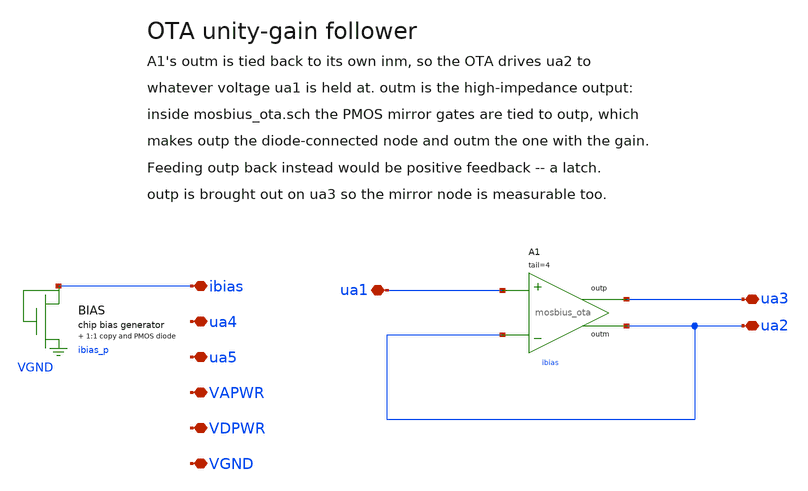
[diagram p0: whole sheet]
** sch_path: examples/otabuf/otabuf.sch
**.subckt otabuf ibias ua1 ua2 ua3 ua4 ua5 VAPWR VDPWR VGND
*.iopin ibias
*.iopin ua1
*.iopin ua2
*.iopin ua3
*.iopin ua4
*.iopin ua5
*.iopin VAPWR
*.iopin VDPWR
*.iopin VGND
XA1 ua1 ua2 ua3 ua2 ibias VGND VAPWR mosbius_ota tail=4
XBIAS ibias ibias_p VGND VAPWR mosbius_bias
**.ends

* expanding   symbol:  mosbius_ota.sym # of pins=4
** sym_path: xschem/mosbius_lib/mosbius_ota.sym
** sch_path: xschem/mosbius_lib/mosbius_ota.sch
.subckt mosbius_ota inp inm outp outm ibias bn bp  tail=2
*.ipin inp
*.ipin inm
*.iopin outp
*.iopin outm
XM3 outp inp net1 bn sky130_fd_pr__nfet_g5v0d10v5 L=0.5 W=40 nf=8 ad='int((nf+1)/2) * W/nf * 0.29' as='int((nf+2)/2) * W/nf * 0.29'
+ pd='2*int((nf+1)/2) * (W/nf + 0.29)' ps='2*int((nf+2)/2) * (W/nf + 0.29)' nrd='0.29 / W' nrs='0.29 / W'
+ sa=0 sb=0 sd=0 mult=1 m=1
XM4 outm inm net1 bn sky130_fd_pr__nfet_g5v0d10v5 L=0.5 W=40 nf=8 ad='int((nf+1)/2) * W/nf * 0.29' as='int((nf+2)/2) * W/nf * 0.29'
+ pd='2*int((nf+1)/2) * (W/nf + 0.29)' ps='2*int((nf+2)/2) * (W/nf + 0.29)' nrd='0.29 / W' nrs='0.29 / W'
+ sa=0 sb=0 sd=0 mult=1 m=1
XM1 outp outp bp bp sky130_fd_pr__pfet_g5v0d10v5 L=1 W=60 nf=8 ad='int((nf+1)/2) * W/nf * 0.29' as='int((nf+2)/2) * W/nf * 0.29'
+ pd='2*int((nf+1)/2) * (W/nf + 0.29)' ps='2*int((nf+2)/2) * (W/nf + 0.29)' nrd='0.29 / W' nrs='0.29 / W'
+ sa=0 sb=0 sd=0 mult=1 m=1
XM2 outm outp bp bp sky130_fd_pr__pfet_g5v0d10v5 L=1 W=60 nf=8 ad='int((nf+1)/2) * W/nf * 0.29' as='int((nf+2)/2) * W/nf * 0.29'
+ pd='2*int((nf+1)/2) * (W/nf + 0.29)' ps='2*int((nf+2)/2) * (W/nf + 0.29)' nrd='0.29 / W' nrs='0.29 / W'
+ sa=0 sb=0 sd=0 mult=1 m=1
XMtail net1 ibias bn mosbius_nsink ratio=tail
* implicit port ibias
.ends


* expanding   symbol:  mosbius_bias.sym # of pins=1
** sym_path: xschem/mosbius_lib/mosbius_bias.sym
** sch_path: xschem/mosbius_lib/mosbius_bias.sch
.subckt mosbius_bias ibias ibias_p bn bp
*.iopin ibias
XMbias_ref ibias ibias bn bn sky130_fd_pr__nfet_g5v0d10v5 L=1 W=10 nf=2 ad='int((nf+1)/2) * W/nf * 0.29'
+ as='int((nf+2)/2) * W/nf * 0.29' pd='2*int((nf+1)/2) * (W/nf + 0.29)' ps='2*int((nf+2)/2) * (W/nf + 0.29)'
+ nrd='0.29 / W' nrs='0.29 / W' sa=0 sb=0 sd=0 mult=1 m=1
XMbias_copy ibias_p ibias bn bn sky130_fd_pr__nfet_g5v0d10v5 L=1 W=10 nf=2 ad='int((nf+1)/2) * W/nf * 0.29'
+ as='int((nf+2)/2) * W/nf * 0.29' pd='2*int((nf+1)/2) * (W/nf + 0.29)' ps='2*int((nf+2)/2) * (W/nf + 0.29)'
+ nrd='0.29 / W' nrs='0.29 / W' sa=0 sb=0 sd=0 mult=1 m=1
XMbias_p ibias_p ibias_p bp bp sky130_fd_pr__pfet_g5v0d10v5 L=1 W=30 nf=30/pmos_width_per_finger ad='int((nf+1)/2) * W/nf * 0.29'
+ as='int((nf+2)/2) * W/nf * 0.29' pd='2*int((nf+1)/2) * (W/nf + 0.29)' ps='2*int((nf+2)/2) * (W/nf + 0.29)'
+ nrd='0.29 / W' nrs='0.29 / W' sa=0 sb=0 sd=0 mult=1 m=1
* implicit port xxx
.ends


* expanding   symbol:  mosbius_nsink.sym # of pins=1
** sym_path: xschem/mosbius_lib/mosbius_nsink.sym
** sch_path: xschem/mosbius_lib/mosbius_nsink.sch
.subckt mosbius_nsink out ibias b  ratio=1
*.iopin ibias
*.iopin b
*.iopin out
XM1 ibias ibias b b sky130_fd_pr__nfet_g5v0d10v5 L=1 W=10 nf=2 ad='int((nf+1)/2) * W/nf * 0.29' as='int((nf+2)/2) * W/nf * 0.29'
+ pd='2*int((nf+1)/2) * (W/nf + 0.29)' ps='2*int((nf+2)/2) * (W/nf + 0.29)' nrd='0.29 / W' nrs='0.29 / W'
+ sa=0 sb=0 sd=0 mult=1 m=1
XM2 out ibias b b sky130_fd_pr__nfet_g5v0d10v5 L=1 W=10*ratio nf=2*ratio ad='int((nf+1)/2) * W/nf * 0.29'
+ as='int((nf+2)/2) * W/nf * 0.29' pd='2*int((nf+1)/2) * (W/nf + 0.29)' ps='2*int((nf+2)/2) * (W/nf + 0.29)'
+ nrd='0.29 / W' nrs='0.29 / W' sa=0 sb=0 sd=0 mult=1 m=1
.ends

.end
